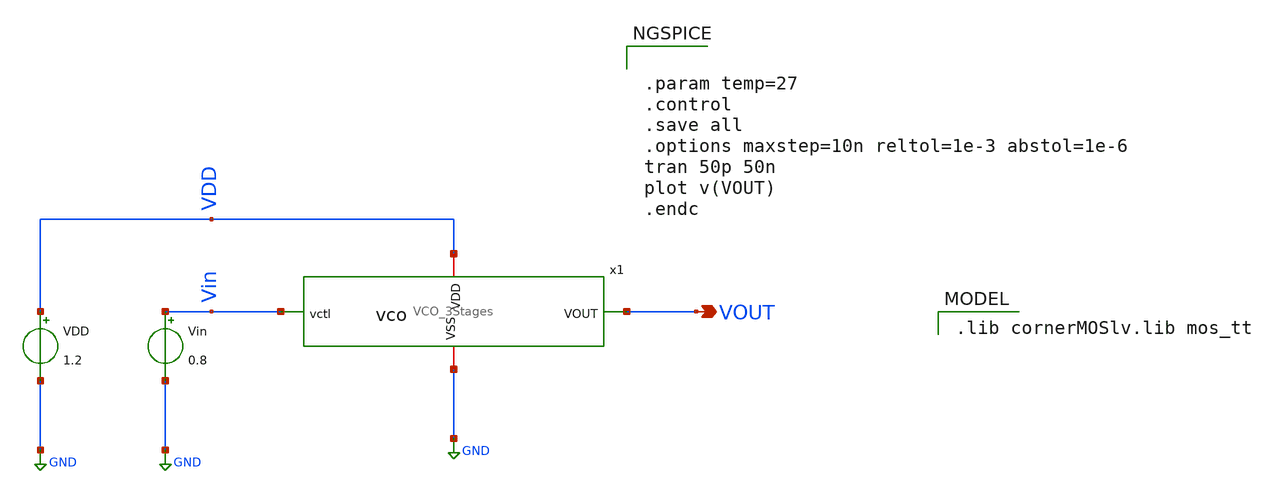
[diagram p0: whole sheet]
** sch_path: Type-II PLL-based Clock Multiplier in 130nm Bi-CMOS Technology/xschem/VCO/VCO_3Stages_tb.sch
**.subckt VCO_3Stages_tb VOUT
*.opin VOUT
VDD VDD GND 1.2
Vin Vin GND 0.8
x1 VDD VOUT Vin GND VCO_3Stages
**** begin user architecture code


.param temp=27
.control
.save all
.options maxstep=10n reltol=1e-3 abstol=1e-6
tran 50p 50n
plot v(VOUT)
.endc


 .lib cornerMOSlv.lib mos_tt

**** end user architecture code
**.ends

* expanding   symbol:  /foss/designs/xschem/VCO/VCO_3Stages.sym # of pins=4
** sym_path: Type-II PLL-based Clock Multiplier in 130nm Bi-CMOS Technology/xschem/VCO/VCO_3Stages.sym
** sch_path: Type-II PLL-based Clock Multiplier in 130nm Bi-CMOS Technology/xschem/VCO/VCO_3Stages.sch
.subckt VCO_3Stages VDD VOUT vctl VSS
*.iopin VDD
*.iopin VSS
*.ipin vctl
*.opin VOUT
XM1 mirror_pg mirror_pg VDD VDD sg13_lv_pmos w=2u l=0.13u ng=1 m=1 mm_ok=1
XM2 net1 mirror_pg VDD VDD sg13_lv_pmos w=2u l=0.13u ng=1 m=1 mm_ok=1
XM3 net2 mirror_pg VDD VDD sg13_lv_pmos w=2u l=0.13u ng=1 m=1 mm_ok=1
XM4 net3 mirror_pg VDD VDD sg13_lv_pmos w=2u l=0.13u ng=1 m=1 mm_ok=1
XM5 mirror_pg vctl VSS VSS sg13_lv_nmos w=1u l=0.13u ng=1 m=1 mm_ok=1
XM6 net6 vctl VSS VSS sg13_lv_nmos w=1u l=0.13u ng=1 m=1 mm_ok=1
XM7 net9 vctl VSS VSS sg13_lv_nmos w=1u l=0.13u ng=1 m=1 mm_ok=1
XM8 net10 vctl VSS VSS sg13_lv_nmos w=1u l=0.13u ng=1 m=1 mm_ok=1
C1 feedback VSS 10f m=1
C2 VOUT VSS 20f m=1
XM9 net4 mirror_pg VDD VDD sg13_lv_pmos w=2u l=0.13u ng=1 m=1 mm_ok=1
XM10 net5 mirror_pg VDD VDD sg13_lv_pmos w=2u l=0.13u ng=1 m=1 mm_ok=1
XM11 net11 vctl VSS VSS sg13_lv_nmos w=1u l=0.13u ng=1 m=1 mm_ok=1
XM12 net14 vctl VSS VSS sg13_lv_nmos w=1u l=0.13u ng=1 m=1 mm_ok=1
x7 net1 feedback net7 net6 t2_vco_nand_inverter
x1 net2 net7 net8 net9 t2_vco_nand_inverter
x2 net3 net8 net12 net10 t2_vco_nand_inverter
x3 net4 net12 net13 net11 t2_vco_nand_inverter
x4 net5 net13 feedback net14 t2_vco_nand_inverter
x5 VDD feedback VOUT VSS t2_vco_nand_inverter
.ends


* expanding   symbol:  /foss/designs/cmos-pll-ihp-sg13g2/Team 2
*+ Design/design_data/xschem/t2_vco_nand_inverter.sym # of pins=4
** sym_path: Type-II PLL-based Clock Multiplier in 130nm Bi-CMOS Technology/xschem/t2_vco_nand_inverter.sym
** sch_path: Type-II PLL-based Clock Multiplier in 130nm Bi-CMOS Technology/xschem/t2_vco_nand_inverter.sch
.subckt t2_vco_nand_inverter VPWR A Y VGND
*.iopin VPWR
*.iopin VGND
*.ipin A
*.opin Y
XM1 Y A VPWR VPWR sg13_lv_pmos w=2u l=0.15u ng=1 m=1 mm_ok=1
XM2 Y A VPWR VPWR sg13_lv_pmos w=2u l=0.13u ng=1 m=1 mm_ok=1
XM3 Y A net1 VGND sg13_lv_nmos w=1u l=0.13u ng=1 m=1 mm_ok=1
XM4 net1 A VGND VGND sg13_lv_nmos w=1u l=0.13u ng=1 m=1 mm_ok=1
.ends

.GLOBAL GND
.end
